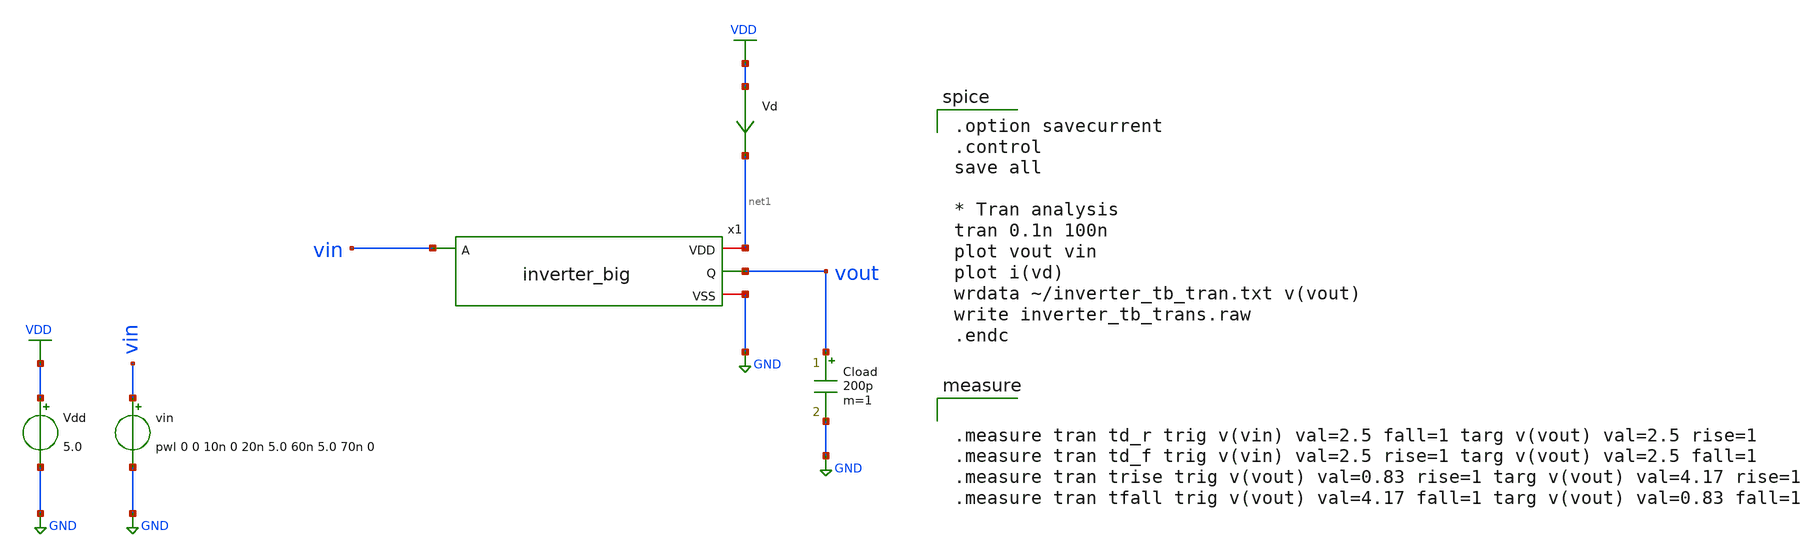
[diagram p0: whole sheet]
** sch_path: inverter/big/inverter_tb_LCap_trans.sch
**.subckt inverter_tb_LCap_trans
Vdd VDD GND 5.0
vin vin GND pwl 0 0 10n 0 20n 5.0 60n 5.0 70n 0
Cload vout GND 200p m=1
Vd VDD net1 0
.save i(vd)
x1 net1 vin vout GND inverter_big
**** begin user architecture code

.option savecurrent
.control
save all

* Tran analysis
tran 0.1n 100n
plot vout vin
plot i(vd)
wrdata ~/inverter_tb_tran.txt v(vout)
write inverter_tb_trans.raw
.endc



.measure tran td_r trig v(vin) val=2.5 fall=1 targ v(vout) val=2.5 rise=1
.measure tran td_f trig v(vin) val=2.5 rise=1 targ v(vout) val=2.5 fall=1
.measure tran trise trig v(vout) val=0.83 rise=1 targ v(vout) val=4.17 rise=1
.measure tran tfall trig v(vout) val=4.17 fall=1 targ v(vout) val=0.83 fall=1


 .include $::LIB/ip62_models
**** end user architecture code
**.ends

* expanding   symbol:  inverter_big.sym # of pins=4
** sym_path: inverter/big/inverter_big.sym
** sch_path: inverter/big/inverter_big.sch
.subckt inverter_big VDD A Q VSS
*.ipin A
*.opin Q
*.iopin VDD
*.iopin VSS
XM1 Q A VDD VDD PMOS w=1600u l=2u as=0 ad=0 ps=0 pd=0 nrd=0 nrs=0 m=1
XM2 Q A VSS VSS NMOS w=680u l=2u as=0 ad=0 ps=0 pd=0 nrd=0 nrs=0 m=1
.ends

.GLOBAL VDD
.GLOBAL GND
.end
